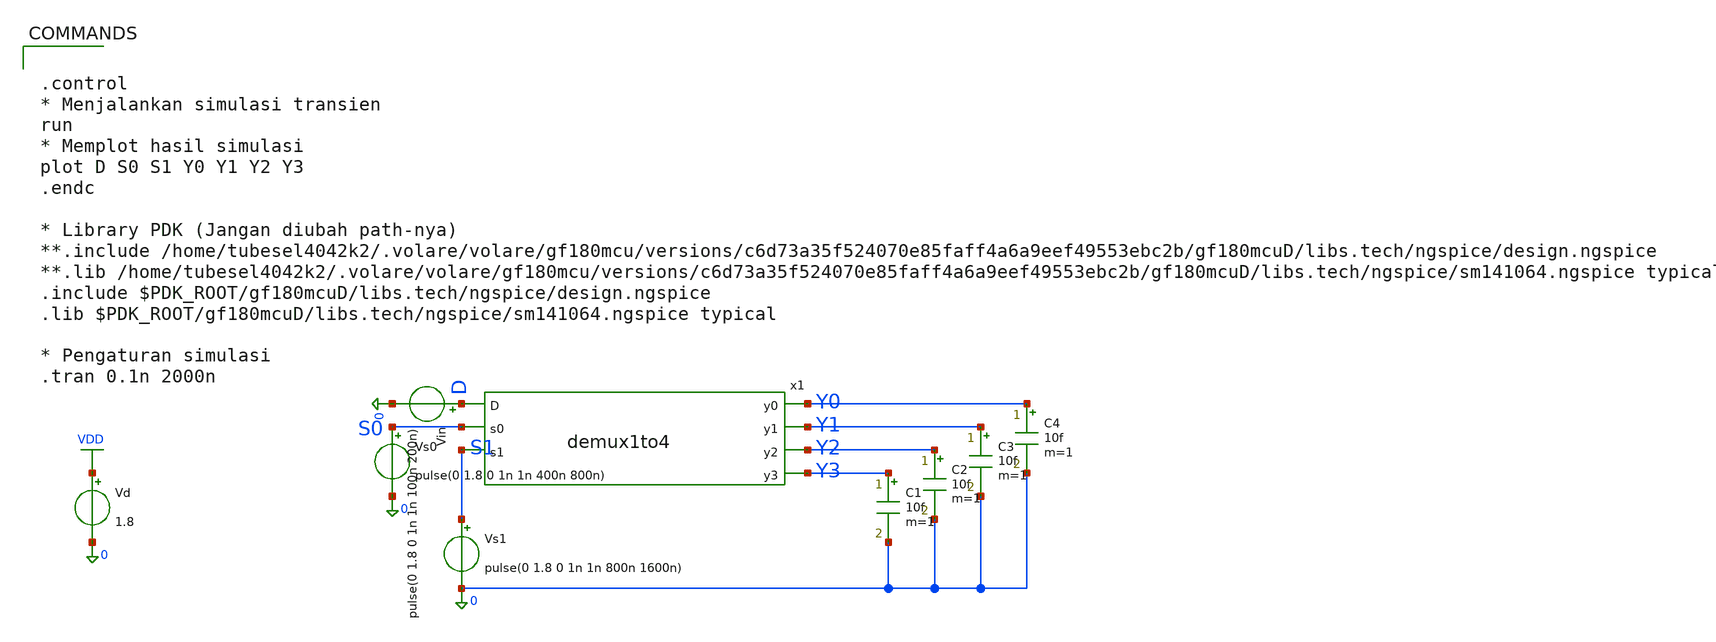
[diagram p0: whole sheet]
** sch_path: src/schematic/DEMUX/tbdemux.sch
**.subckt tbdemux
Vin D 0 pulse(0 1.8 0 1n 1n 100n 200n)
Vs0 S0 0 pulse(0 1.8 0 1n 1n 400n 800n)
Vs1 S1 0 pulse(0 1.8 0 1n 1n 800n 1600n)
Vd VDD 0 1.8
x1 Y0 D S0 Y1 Y2 Y3 S1 demux1to4
C1 Y3 0 10f m=1
C2 Y2 0 10f m=1
C3 Y1 0 10f m=1
C4 Y0 0 10f m=1
**** begin user architecture code


.control
* Menjalankan simulasi transien
run
* Memplot hasil simulasi
plot D S0 S1 Y0 Y1 Y2 Y3
.endc

* Library PDK (Jangan diubah path-nya)
**.include /home/tubesel4042k2/.volare/volare/gf180mcu/versions/c6d73a35f524070e85faff4a6a9eef49553ebc2b/gf180mcuD/libs.tech/ngspice/design.ngspice
**.lib /home/tubesel4042k2/.volare/volare/gf180mcu/versions/c6d73a35f524070e85faff4a6a9eef49553ebc2b/gf180mcuD/libs.tech/ngspice/sm141064.ngspice typical
.include $PDK_ROOT/gf180mcuD/libs.tech/ngspice/design.ngspice
.lib $PDK_ROOT/gf180mcuD/libs.tech/ngspice/sm141064.ngspice typical

* Pengaturan simulasi
.tran 0.1n 2000n


**** end user architecture code
**.ends

* expanding   symbol:  src/schematic/DEMUX/demux1to4.sym # of pins=7
** sym_path: src/schematic/DEMUX/demux1to4.sym
** sch_path: src/schematic/DEMUX/demux1to4.sch
.subckt demux1to4 y0 D s0 y1 y2 y3 s1
*.ipin s0
*.ipin s1
*.ipin D
*.opin y0
*.opin y1
*.opin y2
*.opin y3
x0 VDD s0 s0b 0 inverter
x2 VDD s1 s1b 0 inverter
x3 VDD s1b s0b E0b 0 nand
x4 VDD s1b s0 E1b 0 nand
x5 VDD s1 s0b E2b 0 nand
x6 VDD s1 s0 E3b 0 nand
x7 VDD E0b E0 0 inverter
x8 VDD E1b E1 0 inverter
x9 VDD E2b E2 0 inverter
x10 VDD E3b E3 0 inverter
x11 E0b VDD y0 D 0 E0 transgate
x12 E1b VDD y1 D 0 E1 transgate
x13 E2b VDD y2 D 0 E2 transgate
x14 E3b VDD y3 D 0 E3 transgate
.ends


* expanding   symbol:  inverter.sym # of pins=4
** sym_path: src/schematic/DEMUX/inverter.sym
** sch_path: src/schematic/DEMUX/inverter.sch
.subckt inverter vdd vi vo gnd
*.ipin vi
*.opin vo
*.iopin vdd
*.iopin gnd
XM1 vo vi vdd vdd pfet_03v3 L=0.28u W=0.22u nf=1 ad='int((nf+1)/2) * W/nf * 0.18u' as='int((nf+2)/2) * W/nf * 0.18u'
+ pd='2*int((nf+1)/2) * (W/nf + 0.18u)' ps='2*int((nf+2)/2) * (W/nf + 0.18u)' nrd='0.18u / W' nrs='0.18u / W'
+ sa=0 sb=0 sd=0 m=1
XM2 vo vi gnd gnd nfet_03v3 L=0.28u W=0.22u nf=1 ad='int((nf+1)/2) * W/nf * 0.18u' as='int((nf+2)/2) * W/nf * 0.18u'
+ pd='2*int((nf+1)/2) * (W/nf + 0.18u)' ps='2*int((nf+2)/2) * (W/nf + 0.18u)' nrd='0.18u / W' nrs='0.18u / W'
+ sa=0 sb=0 sd=0 m=1
.ends


* expanding   symbol:  nand.sym # of pins=5
** sym_path: src/schematic/DEMUX/nand.sym
** sch_path: src/schematic/DEMUX/nand.sch
.subckt nand vdd a b y gnd
*.iopin gnd
*.iopin vdd
*.ipin a
*.ipin b
*.opin y
XM1 y a vdd vdd pfet_03v3 L=0.28u W=0.22u nf=1 ad='int((nf+1)/2) * W/nf * 0.18u' as='int((nf+2)/2) * W/nf * 0.18u'
+ pd='2*int((nf+1)/2) * (W/nf + 0.18u)' ps='2*int((nf+2)/2) * (W/nf + 0.18u)' nrd='0.18u / W' nrs='0.18u / W'
+ sa=0 sb=0 sd=0 m=1
XM2 y b vdd vdd pfet_03v3 L=0.28u W=0.22u nf=1 ad='int((nf+1)/2) * W/nf * 0.18u' as='int((nf+2)/2) * W/nf * 0.18u'
+ pd='2*int((nf+1)/2) * (W/nf + 0.18u)' ps='2*int((nf+2)/2) * (W/nf + 0.18u)' nrd='0.18u / W' nrs='0.18u / W'
+ sa=0 sb=0 sd=0 m=1
XM3 y a net1 gnd nfet_03v3 L=0.28u W=0.22u nf=1 ad='int((nf+1)/2) * W/nf * 0.18u' as='int((nf+2)/2) * W/nf * 0.18u'
+ pd='2*int((nf+1)/2) * (W/nf + 0.18u)' ps='2*int((nf+2)/2) * (W/nf + 0.18u)' nrd='0.18u / W' nrs='0.18u / W'
+ sa=0 sb=0 sd=0 m=1
XM4 net1 b gnd gnd nfet_03v3 L=0.28u W=0.22u nf=1 ad='int((nf+1)/2) * W/nf * 0.18u' as='int((nf+2)/2) * W/nf * 0.18u'
+ pd='2*int((nf+1)/2) * (W/nf + 0.18u)' ps='2*int((nf+2)/2) * (W/nf + 0.18u)' nrd='0.18u / W' nrs='0.18u / W'
+ sa=0 sb=0 sd=0 m=1
.ends


* expanding   symbol:  transgate.sym # of pins=6
** sym_path: src/schematic/DEMUX/transgate.sym
** sch_path: src/schematic/DEMUX/transgate.sch
.subckt transgate cb vdd s d gnd c
*.iopin gnd
*.iopin vdd
*.iopin cb
*.iopin c
*.ipin d
*.opin s
XM1 d c s gnd nfet_03v3 L=0.28u W=0.22u nf=1 ad='int((nf+1)/2) * W/nf * 0.18u' as='int((nf+2)/2) * W/nf * 0.18u'
+ pd='2*int((nf+1)/2) * (W/nf + 0.18u)' ps='2*int((nf+2)/2) * (W/nf + 0.18u)' nrd='0.18u / W' nrs='0.18u / W'
+ sa=0 sb=0 sd=0 m=1
XM2 d cb s vdd pfet_03v3 L=0.28u W=0.22u nf=1 ad='int((nf+1)/2) * W/nf * 0.18u' as='int((nf+2)/2) * W/nf * 0.18u'
+ pd='2*int((nf+1)/2) * (W/nf + 0.18u)' ps='2*int((nf+2)/2) * (W/nf + 0.18u)' nrd='0.18u / W' nrs='0.18u / W'
+ sa=0 sb=0 sd=0 m=1
.ends

.GLOBAL VDD
.end
